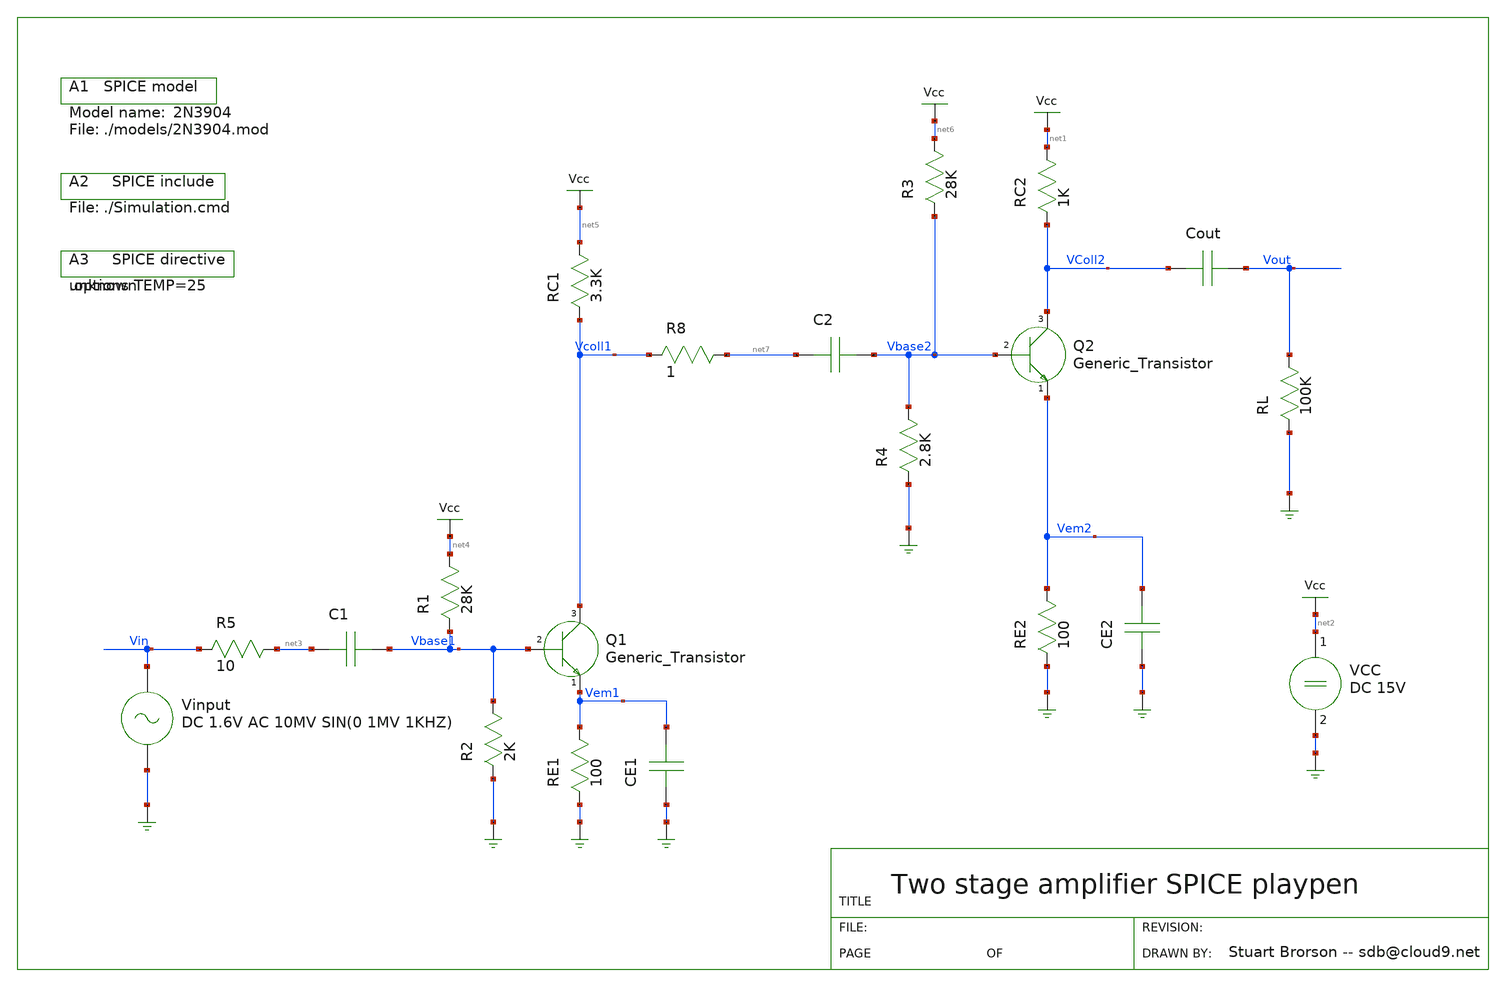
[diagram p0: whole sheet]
** sch_path: xschem_library/gschem_import/TwoStageAmp.sch
**.subckt TwoStageAmp
Q1 Vcoll1 Vem1 Vbase1
R5 Vin net3 10
R1 Vbase1 net4 28K
R2 GND Vbase1 2K
RE1 GND Vem1 100
RC2 VColl2 net1 1K
RL GND Vout 100K
Cout VColl2 Vout 2.2uF
CE1 GND Vem1 1pF
Vinput Vin GND DC 1.6V AC 10MV SIN(0 1MV 1KHZ)
VCC net2 GND DC 15V
A1
.include ./Simulation.cmd
A3 .options TEMP=25
C1 net3 Vbase1 2.2uF
Q2 VColl2 Vem2 Vbase2
RC1 Vcoll1 net5 3.3K
RE2 GND Vem2 100
CE2 GND Vem2 1pF
R8 Vcoll1 net7 1
R3 Vbase2 net6 28K
R4 GND Vbase2 2.8K
C2 net7 Vbase2 2.2uF
**.ends
.end
